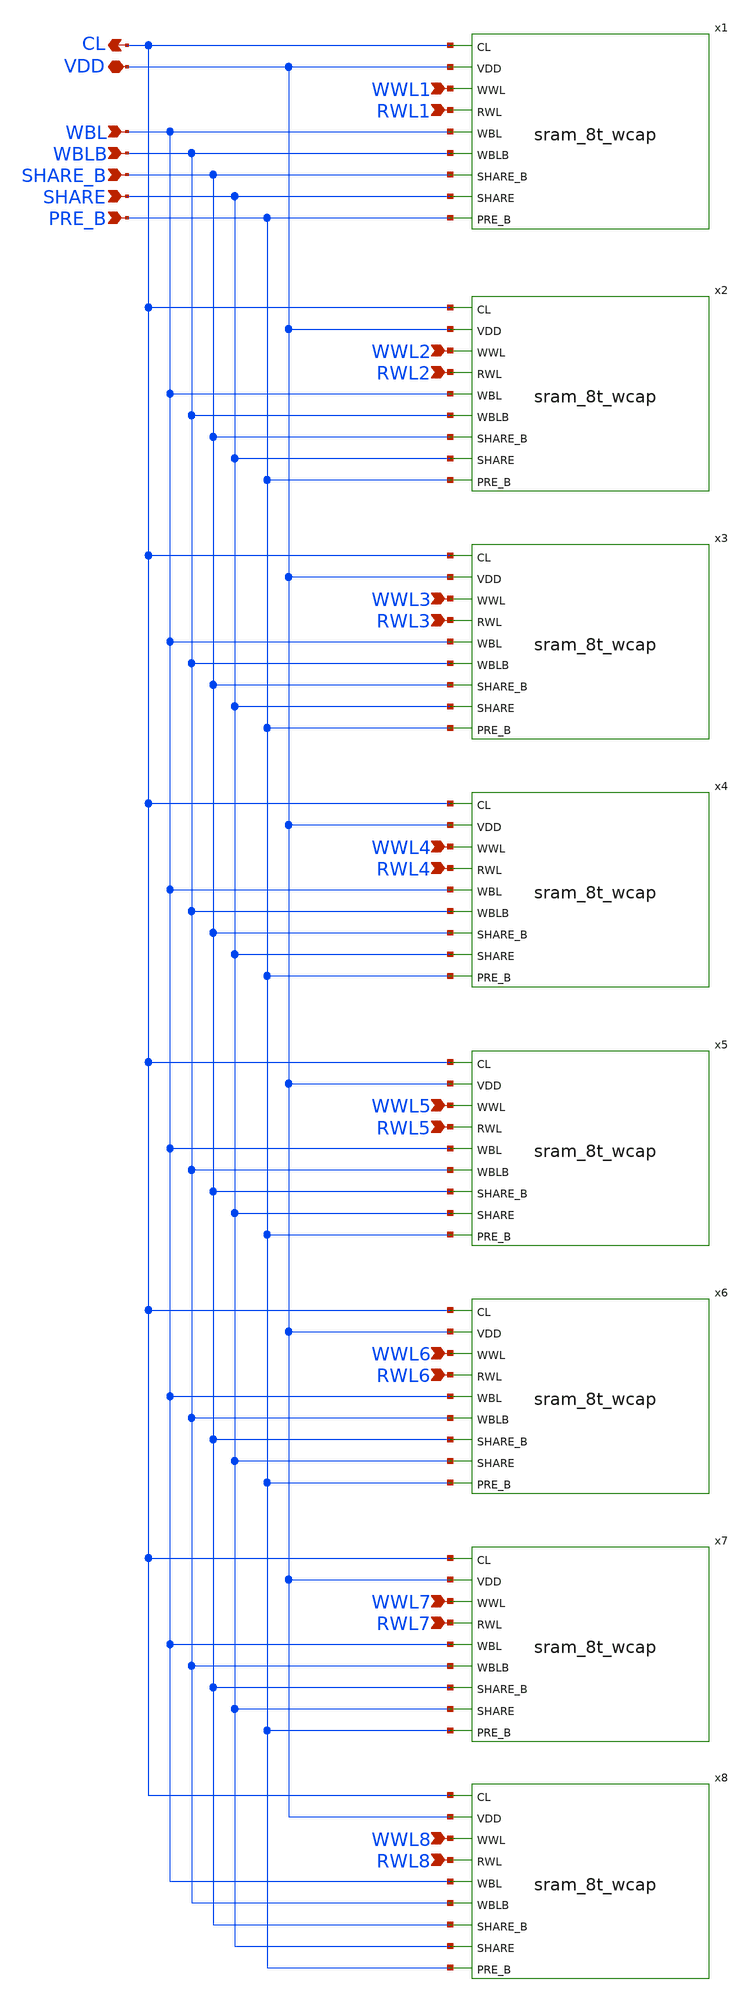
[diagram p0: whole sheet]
** sch_path: schematics/columnt8t_wcap.sch
**.subckt columnt8t_wcap VDD WBL WBLB SHARE_B SHARE PRE_B CL WWL1 RWL1 WWL2 RWL2 WWL3 RWL3 WWL4 RWL4
*+ WWL5 RWL5 WWL6 RWL6 WWL7 RWL7 WWL8 RWL8
*.iopin VDD
*.ipin WBL
*.ipin WBLB
*.ipin SHARE_B
*.ipin SHARE
*.ipin PRE_B
*.opin CL
*.ipin WWL1
*.ipin RWL1
*.ipin WWL2
*.ipin RWL2
*.ipin WWL3
*.ipin RWL3
*.ipin WWL4
*.ipin RWL4
*.ipin WWL5
*.ipin RWL5
*.ipin WWL6
*.ipin RWL6
*.ipin WWL7
*.ipin RWL7
*.ipin WWL8
*.ipin RWL8
x1 CL VDD WWL1 RWL1 WBL WBLB SHARE_B SHARE PRE_B sram_8t_wcap
x2 CL VDD WWL2 RWL2 WBL WBLB SHARE_B SHARE PRE_B sram_8t_wcap
x3 CL VDD WWL3 RWL3 WBL WBLB SHARE_B SHARE PRE_B sram_8t_wcap
x4 CL VDD WWL4 RWL4 WBL WBLB SHARE_B SHARE PRE_B sram_8t_wcap
x5 CL VDD WWL5 RWL5 WBL WBLB SHARE_B SHARE PRE_B sram_8t_wcap
x6 CL VDD WWL6 RWL6 WBL WBLB SHARE_B SHARE PRE_B sram_8t_wcap
x7 CL VDD WWL7 RWL7 WBL WBLB SHARE_B SHARE PRE_B sram_8t_wcap
x8 CL VDD WWL8 RWL8 WBL WBLB SHARE_B SHARE PRE_B sram_8t_wcap
**.ends

* expanding   symbol:  sram_8t_wcap.sym # of pins=9
** sym_path: schematics/sram_8t_wcap.sym
** sch_path: schematics/sram_8t_wcap.sch
.subckt sram_8t_wcap CL VDD WWL RWL WBL WBLB SHARE_B SHARE PRE_B
*.ipin WBLB
*.ipin WBL
*.ipin RWL
*.ipin WWL
*.ipin VDD
*.ipin PRE_B
*.ipin CL
*.ipin SHARE
*.ipin SHARE_B
XM1 0 q qb 0 sky130_fd_pr__nfet_01v8 L=0.15 W=1 nf=1 ad='int((1 + 1)/2) * 1 / 1 * 0.29' as='int((1 + 2)/2) * 1 / 1 * 0.29'
+ pd='2*int((1 + 1)/2) * (1 / 1 + 0.29)' ps='2*int((1 + 2)/2) * (1 / 1 + 0.29)' nrd='0.29 / 1 ' nrs='0.29 / 1 '
+ sa=0 sb=0 sd=0 mult=1 m=1
XM2 VDD q qb VDD sky130_fd_pr__pfet_01v8 L=0.15 W=1 nf=1 ad='int((1 + 1)/2) * 1 / 1 * 0.29' as='int((1 + 2)/2) * 1 / 1 * 0.29'
+ pd='2*int((1 + 1)/2) * (1 / 1 + 0.29)' ps='2*int((1 + 2)/2) * (1 / 1 + 0.29)' nrd='0.29 / 1 ' nrs='0.29 / 1 '
+ sa=0 sb=0 sd=0 mult=1 m=1
XM3 q qb VDD VDD sky130_fd_pr__pfet_01v8 L=0.15 W=1 nf=1 ad='int((1 + 1)/2) * 1 / 1 * 0.29' as='int((1 + 2)/2) * 1 / 1 * 0.29'
+ pd='2*int((1 + 1)/2) * (1 / 1 + 0.29)' ps='2*int((1 + 2)/2) * (1 / 1 + 0.29)' nrd='0.29 / 1 ' nrs='0.29 / 1 '
+ sa=0 sb=0 sd=0 mult=1 m=1
XM4 q qb 0 0 sky130_fd_pr__nfet_01v8 L=0.15 W=1 nf=1 ad='int((1 + 1)/2) * 1 / 1 * 0.29' as='int((1 + 2)/2) * 1 / 1 * 0.29'
+ pd='2*int((1 + 1)/2) * (1 / 1 + 0.29)' ps='2*int((1 + 2)/2) * (1 / 1 + 0.29)' nrd='0.29 / 1 ' nrs='0.29 / 1 '
+ sa=0 sb=0 sd=0 mult=1 m=1
XM5 qb WWL WBLB 0 sky130_fd_pr__nfet_01v8 L=0.15 W=1 nf=1 ad='int((1 + 1)/2) * 1 / 1 * 0.29' as='int((1 + 2)/2) * 1 / 1 * 0.29'
+ pd='2*int((1 + 1)/2) * (1 / 1 + 0.29)' ps='2*int((1 + 2)/2) * (1 / 1 + 0.29)' nrd='0.29 / 1 ' nrs='0.29 / 1 '
+ sa=0 sb=0 sd=0 mult=1 m=1
XM6 WBL WWL q 0 sky130_fd_pr__nfet_01v8 L=0.15 W=1 nf=1 ad='int((1 + 1)/2) * 1 / 1 * 0.29' as='int((1 + 2)/2) * 1 / 1 * 0.29'
+ pd='2*int((1 + 1)/2) * (1 / 1 + 0.29)' ps='2*int((1 + 2)/2) * (1 / 1 + 0.29)' nrd='0.29 / 1 ' nrs='0.29 / 1 '
+ sa=0 sb=0 sd=0 mult=1 m=1
XM7 output q 0 0 sky130_fd_pr__nfet_01v8 L=0.15 W=1 nf=1 ad='int((1 + 1)/2) * 1 / 1 * 0.29' as='int((1 + 2)/2) * 1 / 1 * 0.29'
+ pd='2*int((1 + 1)/2) * (1 / 1 + 0.29)' ps='2*int((1 + 2)/2) * (1 / 1 + 0.29)' nrd='0.29 / 1 ' nrs='0.29 / 1 '
+ sa=0 sb=0 sd=0 mult=1 m=1
XM8 net1 RWL output 0 sky130_fd_pr__nfet_01v8 L=0.15 W=1 nf=1 ad='int((1 + 1)/2) * 1 / 1 * 0.29' as='int((1 + 2)/2) * 1 / 1 * 0.29'
+ pd='2*int((1 + 1)/2) * (1 / 1 + 0.29)' ps='2*int((1 + 2)/2) * (1 / 1 + 0.29)' nrd='0.29 / 1 ' nrs='0.29 / 1 '
+ sa=0 sb=0 sd=0 mult=1 m=1
C1 net1 0 {10f*(1+csig*agauss(0,1,1))} m=1
XM9 CL SHARE net1 0 sky130_fd_pr__nfet_01v8 L=0.15 W=1 nf=1 ad='int((1 + 1)/2) * 1 / 1 * 0.29' as='int((1 + 2)/2) * 1 / 1 * 0.29'
+ pd='2*int((1 + 1)/2) * (1 / 1 + 0.29)' ps='2*int((1 + 2)/2) * (1 / 1 + 0.29)' nrd='0.29 / 1 ' nrs='0.29 / 1 '
+ sa=0 sb=0 sd=0 mult=1 m=1
XM10 net1 PRE_B VDD VDD sky130_fd_pr__pfet_01v8 L=0.15 W=1 nf=1 ad='int((1 + 1)/2) * 1 / 1 * 0.29' as='int((1 + 2)/2) * 1 / 1 * 0.29'
+ pd='2*int((1 + 1)/2) * (1 / 1 + 0.29)' ps='2*int((1 + 2)/2) * (1 / 1 + 0.29)' nrd='0.29 / 1 ' nrs='0.29 / 1 '
+ sa=0 sb=0 sd=0 mult=1 m=1
XM11 CL SHARE_B net1 VDD sky130_fd_pr__pfet_01v8 L=0.15 W=1 nf=1 ad='int((1 + 1)/2) * 1 / 1 * 0.29' as='int((1 + 2)/2) * 1 / 1 * 0.29'
+ pd='2*int((1 + 1)/2) * (1 / 1 + 0.29)' ps='2*int((1 + 2)/2) * (1 / 1 + 0.29)' nrd='0.29 / 1 ' nrs='0.29 / 1 '
+ sa=0 sb=0 sd=0 mult=1 m=1
.ends

.end
